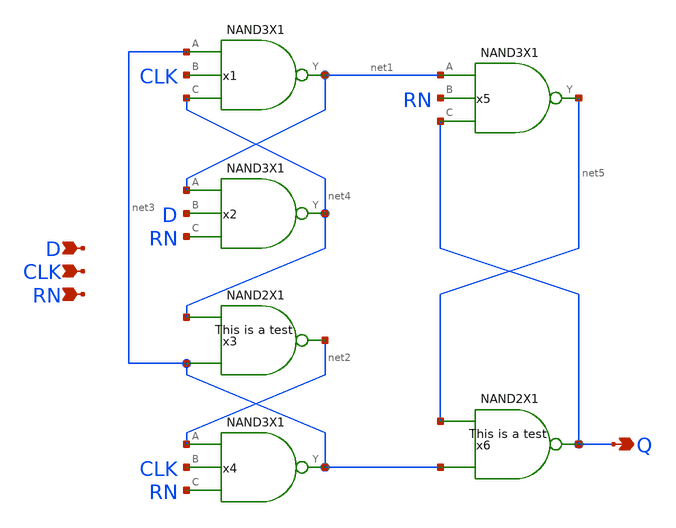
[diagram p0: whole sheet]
** sch_path: archives/lib/xschem/DFFRNQX1.sch
**.subckt DFFRNQX1 Q D CLK RN
*.opin Q
*.ipin D
*.ipin CLK
*.ipin RN
x2 net4 net1 D RN VDD VSS NAND3X1
x1 net1 net3 CLK net4 VDD VSS NAND3X1
x3 net2 net4 net3 VDD VSS NAND2X1
x4 net3 net2 CLK RN VDD VSS NAND3X1
x5 net5 net1 RN Q VDD VSS NAND3X1
x6 Q net5 net3 VDD VSS NAND2X1
**.ends
.end
